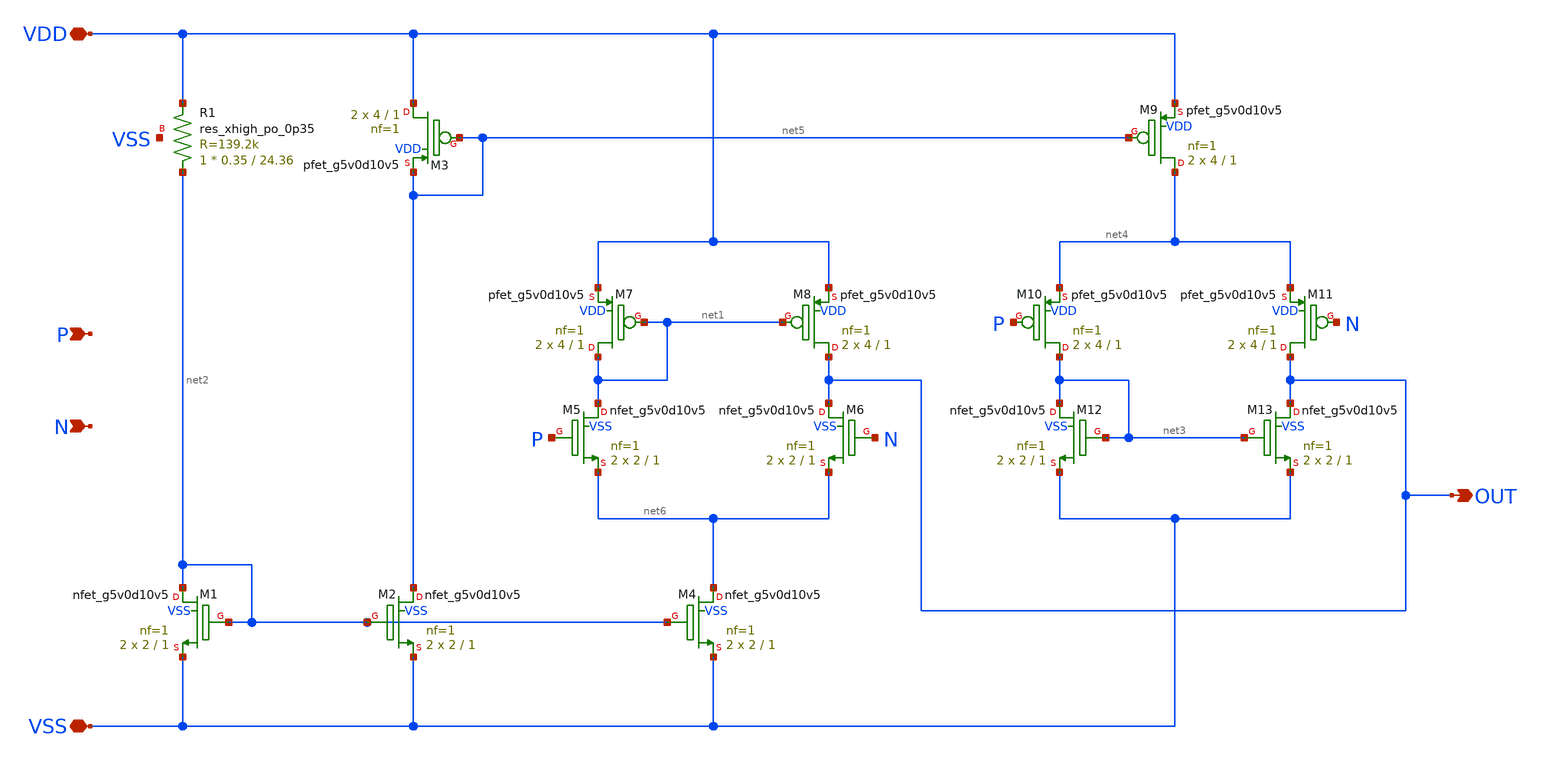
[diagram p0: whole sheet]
** sch_path: xschem/opamp.sch
**.subckt opamp VDD VSS P N OUT
*.iopin VDD
*.iopin VSS
*.ipin P
*.ipin N
*.opin OUT
XR1 net2 VDD VSS sky130_fd_pr__res_xhigh_po_0p35 L=24.36 mult=1 m=1
XM1 net2 net2 VSS VSS sky130_fd_pr__nfet_g5v0d10v5 L=1 W=2 nf=1 ad='int((nf+1)/2) * W/nf * 0.29' as='int((nf+2)/2) * W/nf * 0.29'
+ pd='2*int((nf+1)/2) * (W/nf + 0.29)' ps='2*int((nf+2)/2) * (W/nf + 0.29)' nrd='0.29 / W' nrs='0.29 / W'
+ sa=0 sb=0 sd=0 mult=2 m=2
XM7 net1 net1 VDD VDD sky130_fd_pr__pfet_g5v0d10v5 L=1 W=4 nf=1 ad='int((nf+1)/2) * W/nf * 0.29' as='int((nf+2)/2) * W/nf * 0.29'
+ pd='2*int((nf+1)/2) * (W/nf + 0.29)' ps='2*int((nf+2)/2) * (W/nf + 0.29)' nrd='0.29 / W' nrs='0.29 / W'
+ sa=0 sb=0 sd=0 mult=2 m=2
XM8 OUT net1 VDD VDD sky130_fd_pr__pfet_g5v0d10v5 L=1 W=4 nf=1 ad='int((nf+1)/2) * W/nf * 0.29' as='int((nf+2)/2) * W/nf * 0.29'
+ pd='2*int((nf+1)/2) * (W/nf + 0.29)' ps='2*int((nf+2)/2) * (W/nf + 0.29)' nrd='0.29 / W' nrs='0.29 / W'
+ sa=0 sb=0 sd=0 mult=2 m=2
XM4 net6 net2 VSS VSS sky130_fd_pr__nfet_g5v0d10v5 L=1 W=2 nf=1 ad='int((nf+1)/2) * W/nf * 0.29' as='int((nf+2)/2) * W/nf * 0.29'
+ pd='2*int((nf+1)/2) * (W/nf + 0.29)' ps='2*int((nf+2)/2) * (W/nf + 0.29)' nrd='0.29 / W' nrs='0.29 / W'
+ sa=0 sb=0 sd=0 mult=2 m=2
XM5 net1 P net6 VSS sky130_fd_pr__nfet_g5v0d10v5 L=1 W=2 nf=1 ad='int((nf+1)/2) * W/nf * 0.29' as='int((nf+2)/2) * W/nf * 0.29'
+ pd='2*int((nf+1)/2) * (W/nf + 0.29)' ps='2*int((nf+2)/2) * (W/nf + 0.29)' nrd='0.29 / W' nrs='0.29 / W'
+ sa=0 sb=0 sd=0 mult=2 m=2
XM6 OUT N net6 VSS sky130_fd_pr__nfet_g5v0d10v5 L=1 W=2 nf=1 ad='int((nf+1)/2) * W/nf * 0.29' as='int((nf+2)/2) * W/nf * 0.29'
+ pd='2*int((nf+1)/2) * (W/nf + 0.29)' ps='2*int((nf+2)/2) * (W/nf + 0.29)' nrd='0.29 / W' nrs='0.29 / W'
+ sa=0 sb=0 sd=0 mult=2 m=2
XM2 net5 net2 VSS VSS sky130_fd_pr__nfet_g5v0d10v5 L=1 W=2 nf=1 ad='int((nf+1)/2) * W/nf * 0.29' as='int((nf+2)/2) * W/nf * 0.29'
+ pd='2*int((nf+1)/2) * (W/nf + 0.29)' ps='2*int((nf+2)/2) * (W/nf + 0.29)' nrd='0.29 / W' nrs='0.29 / W'
+ sa=0 sb=0 sd=0 mult=2 m=2
XM9 net4 net5 VDD VDD sky130_fd_pr__pfet_g5v0d10v5 L=1 W=4 nf=1 ad='int((nf+1)/2) * W/nf * 0.29' as='int((nf+2)/2) * W/nf * 0.29'
+ pd='2*int((nf+1)/2) * (W/nf + 0.29)' ps='2*int((nf+2)/2) * (W/nf + 0.29)' nrd='0.29 / W' nrs='0.29 / W'
+ sa=0 sb=0 sd=0 mult=2 m=2
XM3 VDD net5 net5 VDD sky130_fd_pr__pfet_g5v0d10v5 L=1 W=4 nf=1 ad='int((nf+1)/2) * W/nf * 0.29' as='int((nf+2)/2) * W/nf * 0.29'
+ pd='2*int((nf+1)/2) * (W/nf + 0.29)' ps='2*int((nf+2)/2) * (W/nf + 0.29)' nrd='0.29 / W' nrs='0.29 / W'
+ sa=0 sb=0 sd=0 mult=2 m=2
XM10 net3 P net4 VDD sky130_fd_pr__pfet_g5v0d10v5 L=1 W=4 nf=1 ad='int((nf+1)/2) * W/nf * 0.29' as='int((nf+2)/2) * W/nf * 0.29'
+ pd='2*int((nf+1)/2) * (W/nf + 0.29)' ps='2*int((nf+2)/2) * (W/nf + 0.29)' nrd='0.29 / W' nrs='0.29 / W'
+ sa=0 sb=0 sd=0 mult=2 m=2
XM11 OUT N net4 VDD sky130_fd_pr__pfet_g5v0d10v5 L=1 W=4 nf=1 ad='int((nf+1)/2) * W/nf * 0.29' as='int((nf+2)/2) * W/nf * 0.29'
+ pd='2*int((nf+1)/2) * (W/nf + 0.29)' ps='2*int((nf+2)/2) * (W/nf + 0.29)' nrd='0.29 / W' nrs='0.29 / W'
+ sa=0 sb=0 sd=0 mult=2 m=2
XM12 net3 net3 VSS VSS sky130_fd_pr__nfet_g5v0d10v5 L=1 W=2 nf=1 ad='int((nf+1)/2) * W/nf * 0.29' as='int((nf+2)/2) * W/nf * 0.29'
+ pd='2*int((nf+1)/2) * (W/nf + 0.29)' ps='2*int((nf+2)/2) * (W/nf + 0.29)' nrd='0.29 / W' nrs='0.29 / W'
+ sa=0 sb=0 sd=0 mult=2 m=2
XM13 OUT net3 VSS VSS sky130_fd_pr__nfet_g5v0d10v5 L=1 W=2 nf=1 ad='int((nf+1)/2) * W/nf * 0.29' as='int((nf+2)/2) * W/nf * 0.29'
+ pd='2*int((nf+1)/2) * (W/nf + 0.29)' ps='2*int((nf+2)/2) * (W/nf + 0.29)' nrd='0.29 / W' nrs='0.29 / W'
+ sa=0 sb=0 sd=0 mult=2 m=2
**.ends
.end
